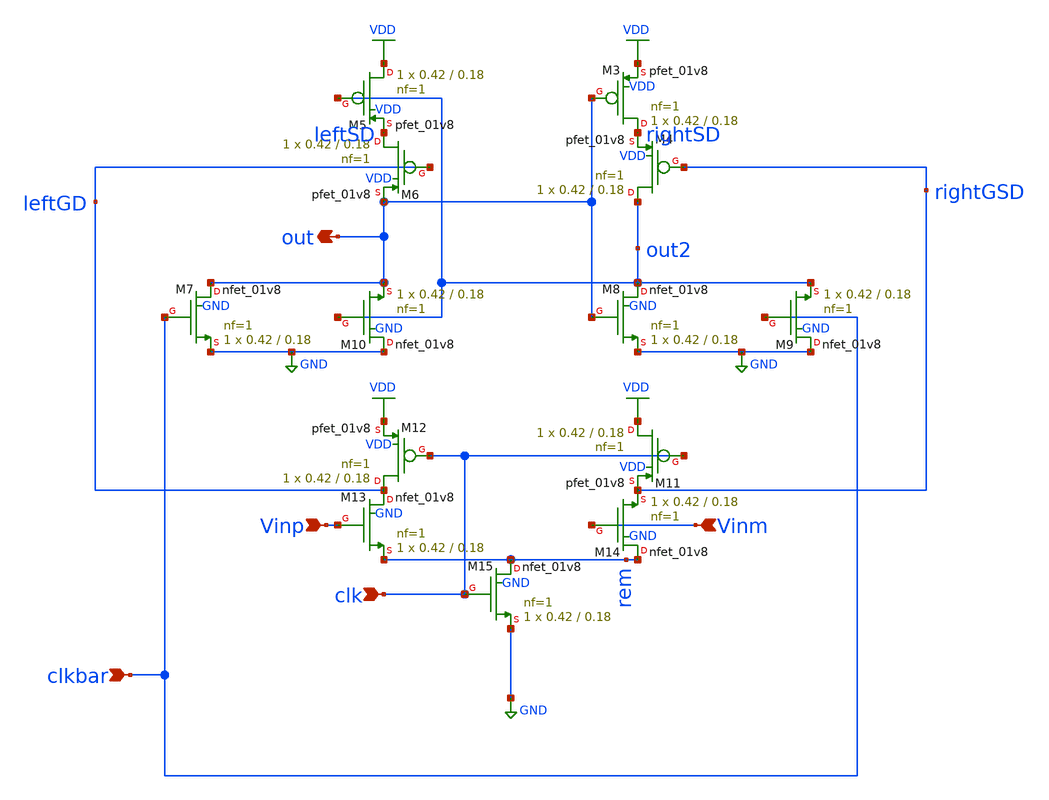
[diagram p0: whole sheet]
** sch_path: xschem/comparator/doubletaillatch.sch
**.subckt doubletaillatch clkbar out Vinp Vinm clk
*.ipin clkbar
*.opin out
*.ipin Vinp
*.ipin Vinm
*.ipin clk
XM3 rightSD out VDD VDD sky130_fd_pr__pfet_01v8 L=0.18 W=0.42 nf=1 ad='int((nf+1)/2) * W/nf * 0.29' as='int((nf+2)/2) * W/nf * 0.29'
+ pd='2*int((nf+1)/2) * (W/nf + 0.29)' ps='2*int((nf+2)/2) * (W/nf + 0.29)' nrd='0.29 / W' nrs='0.29 / W'
+ sa=0 sb=0 sd=0 mult=1 m=1
XM4 out2 rightGSD rightSD VDD sky130_fd_pr__pfet_01v8 L=0.18 W=0.42 nf=1 ad='int((nf+1)/2) * W/nf * 0.29'
+ as='int((nf+2)/2) * W/nf * 0.29' pd='2*int((nf+1)/2) * (W/nf + 0.29)' ps='2*int((nf+2)/2) * (W/nf + 0.29)'
+ nrd='0.29 / W' nrs='0.29 / W' sa=0 sb=0 sd=0 mult=1 m=1
XM5 VDD out2 leftSD VDD sky130_fd_pr__pfet_01v8 L=0.18 W=0.42 nf=1 ad='int((nf+1)/2) * W/nf * 0.29' as='int((nf+2)/2) * W/nf * 0.29'
+ pd='2*int((nf+1)/2) * (W/nf + 0.29)' ps='2*int((nf+2)/2) * (W/nf + 0.29)' nrd='0.29 / W' nrs='0.29 / W'
+ sa=0 sb=0 sd=0 mult=1 m=1
XM6 leftSD leftGD out VDD sky130_fd_pr__pfet_01v8 L=0.18 W=0.42 nf=1 ad='int((nf+1)/2) * W/nf * 0.29'
+ as='int((nf+2)/2) * W/nf * 0.29' pd='2*int((nf+1)/2) * (W/nf + 0.29)' ps='2*int((nf+2)/2) * (W/nf + 0.29)'
+ nrd='0.29 / W' nrs='0.29 / W' sa=0 sb=0 sd=0 mult=1 m=1
XM11 VDD clk rightGSD VDD sky130_fd_pr__pfet_01v8 L=0.18 W=0.42 nf=1 ad='int((nf+1)/2) * W/nf * 0.29'
+ as='int((nf+2)/2) * W/nf * 0.29' pd='2*int((nf+1)/2) * (W/nf + 0.29)' ps='2*int((nf+2)/2) * (W/nf + 0.29)'
+ nrd='0.29 / W' nrs='0.29 / W' sa=0 sb=0 sd=0 mult=1 m=1
XM12 leftGD clk VDD VDD sky130_fd_pr__pfet_01v8 L=0.18 W=0.42 nf=1 ad='int((nf+1)/2) * W/nf * 0.29' as='int((nf+2)/2) * W/nf * 0.29'
+ pd='2*int((nf+1)/2) * (W/nf + 0.29)' ps='2*int((nf+2)/2) * (W/nf + 0.29)' nrd='0.29 / W' nrs='0.29 / W'
+ sa=0 sb=0 sd=0 mult=1 m=1
XM7 out clkbar GND GND sky130_fd_pr__nfet_01v8 L=0.18 W=0.42 nf=1 ad='int((nf+1)/2) * W/nf * 0.29' as='int((nf+2)/2) * W/nf * 0.29'
+ pd='2*int((nf+1)/2) * (W/nf + 0.29)' ps='2*int((nf+2)/2) * (W/nf + 0.29)' nrd='0.29 / W' nrs='0.29 / W'
+ sa=0 sb=0 sd=0 mult=1 m=1
XM8 out2 out GND GND sky130_fd_pr__nfet_01v8 L=0.18 W=0.42 nf=1 ad='int((nf+1)/2) * W/nf * 0.29' as='int((nf+2)/2) * W/nf * 0.29'
+ pd='2*int((nf+1)/2) * (W/nf + 0.29)' ps='2*int((nf+2)/2) * (W/nf + 0.29)' nrd='0.29 / W' nrs='0.29 / W'
+ sa=0 sb=0 sd=0 mult=1 m=1
XM9 GND clkbar out2 GND sky130_fd_pr__nfet_01v8 L=0.18 W=0.42 nf=1 ad='int((nf+1)/2) * W/nf * 0.29' as='int((nf+2)/2) * W/nf * 0.29'
+ pd='2*int((nf+1)/2) * (W/nf + 0.29)' ps='2*int((nf+2)/2) * (W/nf + 0.29)' nrd='0.29 / W' nrs='0.29 / W'
+ sa=0 sb=0 sd=0 mult=1 m=1
XM10 GND out2 out GND sky130_fd_pr__nfet_01v8 L=0.18 W=0.42 nf=1 ad='int((nf+1)/2) * W/nf * 0.29' as='int((nf+2)/2) * W/nf * 0.29'
+ pd='2*int((nf+1)/2) * (W/nf + 0.29)' ps='2*int((nf+2)/2) * (W/nf + 0.29)' nrd='0.29 / W' nrs='0.29 / W'
+ sa=0 sb=0 sd=0 mult=1 m=1
XM13 leftGD Vinp rem GND sky130_fd_pr__nfet_01v8 L=0.18 W=0.42 nf=1 ad='int((nf+1)/2) * W/nf * 0.29'
+ as='int((nf+2)/2) * W/nf * 0.29' pd='2*int((nf+1)/2) * (W/nf + 0.29)' ps='2*int((nf+2)/2) * (W/nf + 0.29)'
+ nrd='0.29 / W' nrs='0.29 / W' sa=0 sb=0 sd=0 mult=1 m=1
XM14 rem Vinm rightGSD GND sky130_fd_pr__nfet_01v8 L=0.18 W=0.42 nf=1 ad='int((nf+1)/2) * W/nf * 0.29'
+ as='int((nf+2)/2) * W/nf * 0.29' pd='2*int((nf+1)/2) * (W/nf + 0.29)' ps='2*int((nf+2)/2) * (W/nf + 0.29)'
+ nrd='0.29 / W' nrs='0.29 / W' sa=0 sb=0 sd=0 mult=1 m=1
XM15 rem clk GND GND sky130_fd_pr__nfet_01v8 L=0.18 W=0.42 nf=1 ad='int((nf+1)/2) * W/nf * 0.29' as='int((nf+2)/2) * W/nf * 0.29'
+ pd='2*int((nf+1)/2) * (W/nf + 0.29)' ps='2*int((nf+2)/2) * (W/nf + 0.29)' nrd='0.29 / W' nrs='0.29 / W'
+ sa=0 sb=0 sd=0 mult=1 m=1
**.ends
.GLOBAL VDD
.GLOBAL GND
.end
